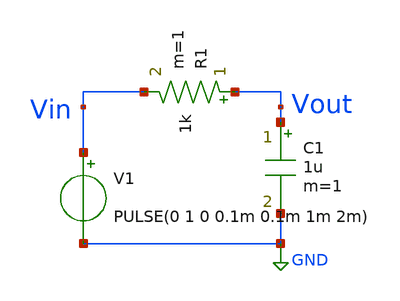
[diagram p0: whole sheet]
** sch_path: test.sch
**.subckt test
R1 Vout Vin 1k m=1
C1 Vout GND 1u m=1
V1 Vin GND PULSE(0 1 0 0.1m 0.1m 1m 2m)
**** begin user architecture code


.tran 1u 10m
.save all


**** end user architecture code
**.ends
.GLOBAL GND
.end
